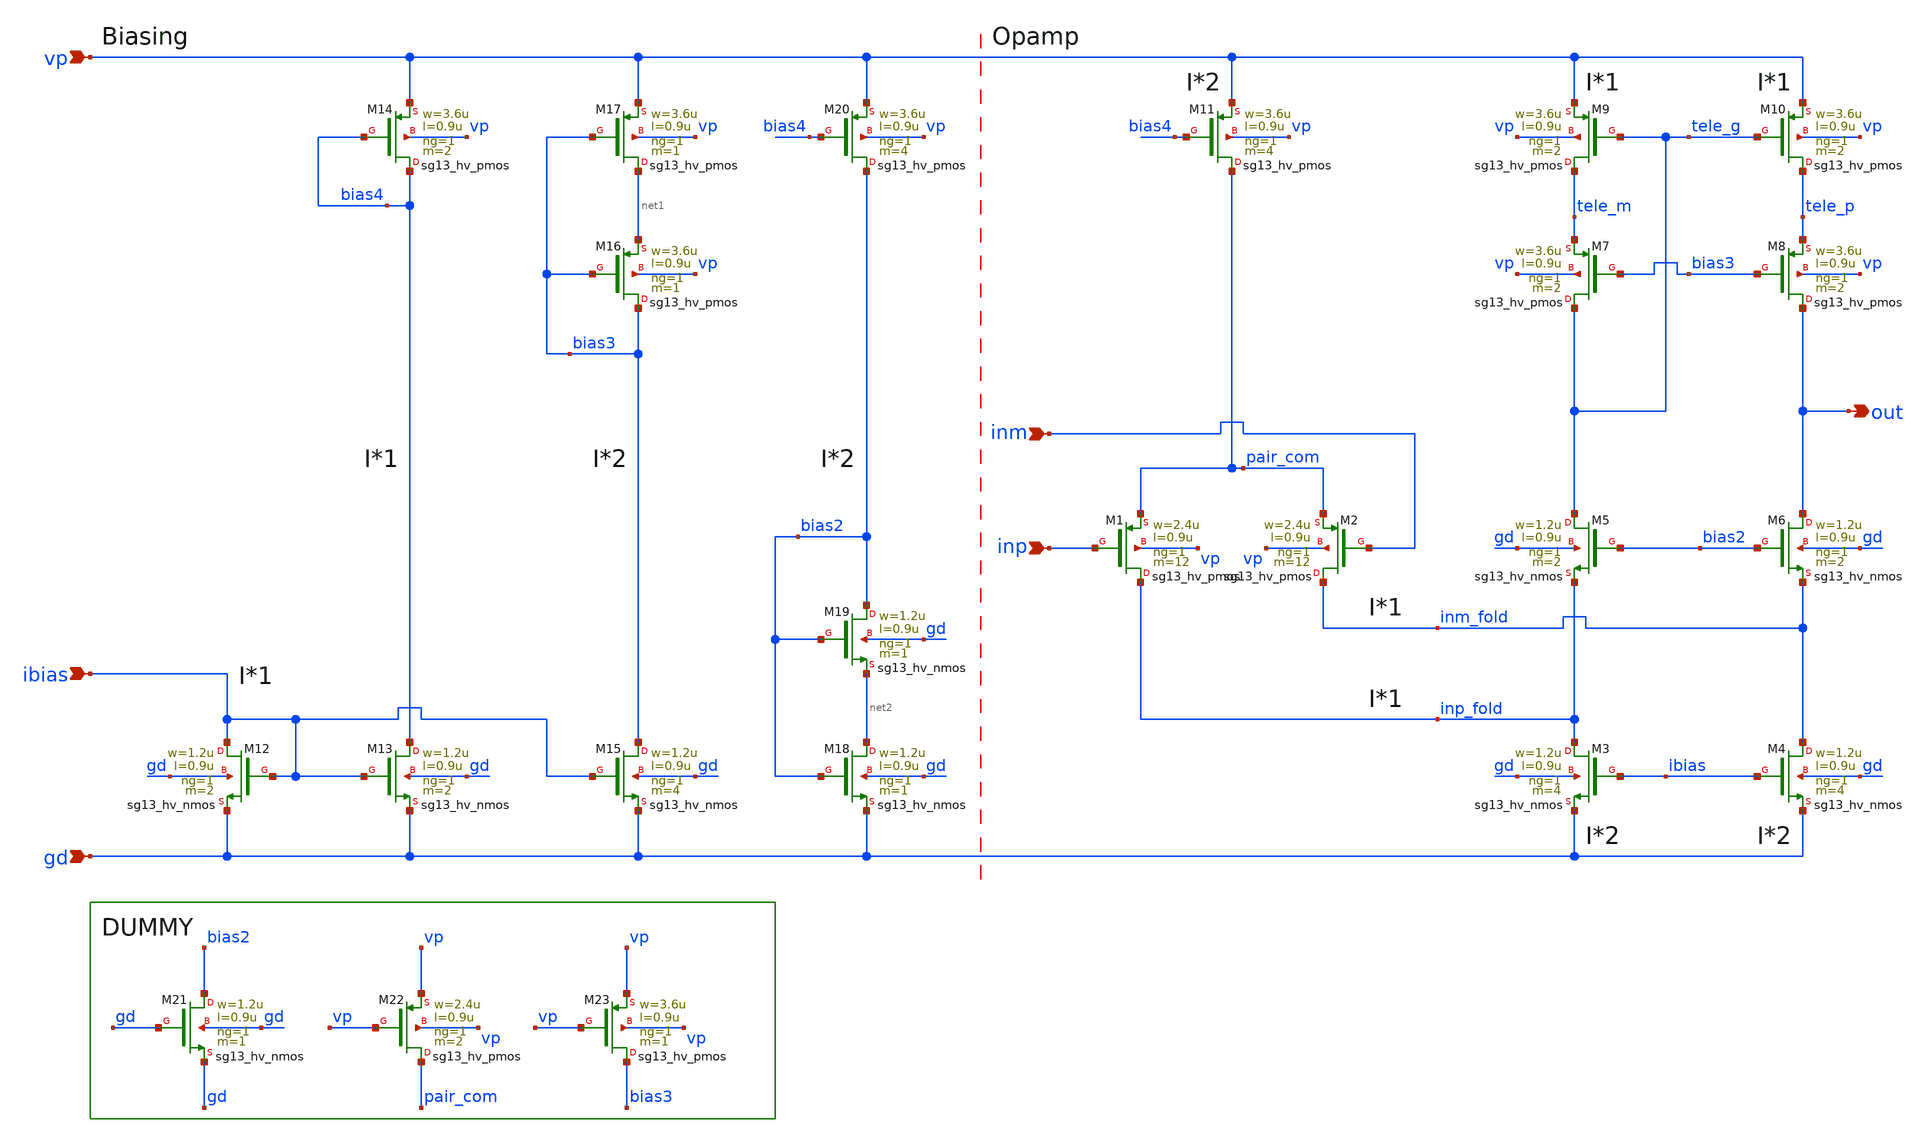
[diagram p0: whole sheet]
** sch_path: PLL0663-main/schematic/xschem/bandgap/opamp_folded_pmos.sch
**.subckt opamp_folded_pmos ibias inp inm out gd vp
*.ipin ibias
*.ipin inp
*.ipin inm
*.opin out
*.ipin gd
*.ipin vp
XM13 bias4 ibias gd gd sg13_hv_nmos w=1.2u l=0.9u ng=1 m=2 mm_ok=1
XM12 ibias ibias gd gd sg13_hv_nmos w=1.2u l=0.9u ng=1 m=2 mm_ok=1
XM14 bias4 bias4 vp vp sg13_hv_pmos w=3.6u l=0.9u ng=1 m=2 mm_ok=1
XM11 pair_com bias4 vp vp sg13_hv_pmos w=3.6u l=0.9u ng=1 m=4 mm_ok=1
XM1 inp_fold inp pair_com vp sg13_hv_pmos w=2.4u l=0.9u ng=1 m=12 mm_ok=1
XM2 inm_fold inm pair_com vp sg13_hv_pmos w=2.4u l=0.9u ng=1 m=12 mm_ok=1
XM9 tele_m tele_g vp vp sg13_hv_pmos w=3.6u l=0.9u ng=1 m=2 mm_ok=1
XM10 tele_p tele_g vp vp sg13_hv_pmos w=3.6u l=0.9u ng=1 m=2 mm_ok=1
XM7 tele_g bias3 tele_m vp sg13_hv_pmos w=3.6u l=0.9u ng=1 m=2 mm_ok=1
XM8 out bias3 tele_p vp sg13_hv_pmos w=3.6u l=0.9u ng=1 m=2 mm_ok=1
XM3 inp_fold ibias gd gd sg13_hv_nmos w=1.2u l=0.9u ng=1 m=4 mm_ok=1
XM4 inm_fold ibias gd gd sg13_hv_nmos w=1.2u l=0.9u ng=1 m=4 mm_ok=1
XM5 tele_g bias2 inp_fold gd sg13_hv_nmos w=1.2u l=0.9u ng=1 m=2 mm_ok=1
XM6 out bias2 inm_fold gd sg13_hv_nmos w=1.2u l=0.9u ng=1 m=2 mm_ok=1
XM15 bias3 ibias gd gd sg13_hv_nmos w=1.2u l=0.9u ng=1 m=4 mm_ok=1
XM16 bias3 bias3 net1 vp sg13_hv_pmos w=3.6u l=0.9u ng=1 m=1 mm_ok=1
XM17 net1 bias3 vp vp sg13_hv_pmos w=3.6u l=0.9u ng=1 m=1 mm_ok=1
XM20 bias2 bias4 vp vp sg13_hv_pmos w=3.6u l=0.9u ng=1 m=4 mm_ok=1
XM18 net2 bias2 gd gd sg13_hv_nmos w=1.2u l=0.9u ng=1 m=1 mm_ok=1
XM19 bias2 bias2 net2 gd sg13_hv_nmos w=1.2u l=0.9u ng=1 m=1 mm_ok=1
XM21 bias2 gd gd gd sg13_hv_nmos w=1.2u l=0.9u ng=1 m=1 mm_ok=1
XM22 pair_com vp vp vp sg13_hv_pmos w=2.4u l=0.9u ng=1 m=2 mm_ok=1
XM23 bias3 vp vp vp sg13_hv_pmos w=3.6u l=0.9u ng=1 m=1 mm_ok=1
**.ends
.end
